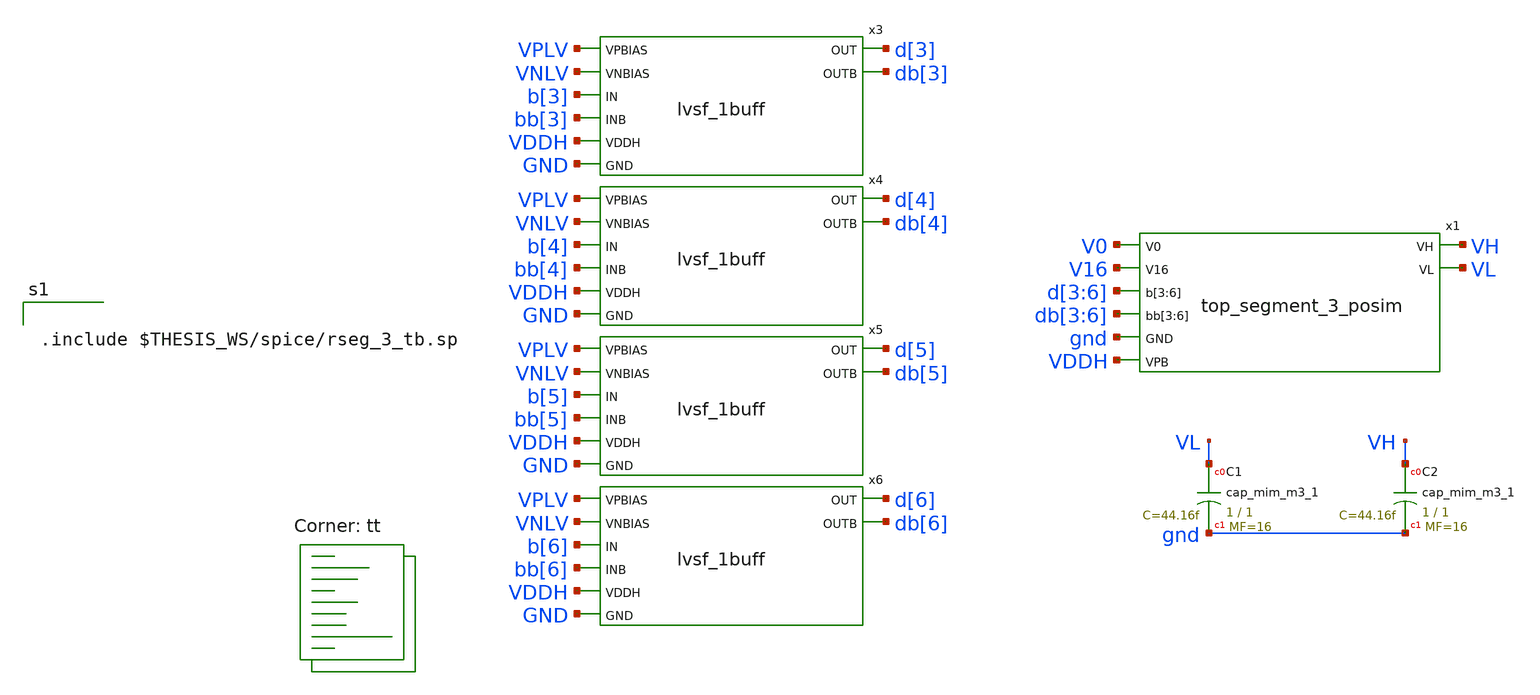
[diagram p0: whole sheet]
** sch_path: xschem/res_seg_3-tb.sch
**.subckt res_seg_3-tb
XC1 VL gnd sky130_fd_pr__cap_mim_m3_1 W=1 L=1 MF=16 m=16
XC2 VH gnd sky130_fd_pr__cap_mim_m3_1 W=1 L=1 MF=16 m=16
x3 VPLV VNLV b[3] bb[3] d[3] db[3] VDDH GND lvsf_1buff
x4 VPLV VNLV b[4] bb[4] d[4] db[4] VDDH GND lvsf_1buff
x5 VPLV VNLV b[5] bb[5] d[5] db[5] VDDH GND lvsf_1buff
x6 VPLV VNLV b[6] bb[6] d[6] db[6] VDDH GND lvsf_1buff
x1 V0 V16 d[3] d[4] d[5] d[6] db[3] db[4] db[5] db[6] VH VL gnd VDDH top_segment_3_posim
**** begin user architecture code
.lib $::SKYWATER_MODELS/sky130.lib.spice tt


.include $THESIS_WS/spice/rseg_3_tb.sp

**** end user architecture code
**.ends

* expanding   symbol:  lvsf_1buff.sym # of pins=8
** sym_path: xschem/lvsf_1buff.sym
** sch_path: xschem/lvsf_1buff.sch
.subckt lvsf_1buff VPBIAS VNBIAS IN INB OUT OUTB VDDH GND
*.ipin IN
*.ipin INB
*.opin OUT
*.ipin VDDH
*.ipin GND
*.ipin VPBIAS
*.ipin VNBIAS
*.opin OUTB
XM13 n1 IN GND GND sky130_fd_pr__nfet_01v8 L=0.15 W=3 nf=1 ad='int((nf+1)/2) * W/nf * 0.29' as='int((nf+2)/2) * W/nf * 0.29'
+ pd='2*int((nf+1)/2) * (W/nf + 0.29)' ps='2*int((nf+2)/2) * (W/nf + 0.29)' nrd='0.29 / W' nrs='0.29 / W'
+ sa=0 sb=0 sd=0 mult=1 m=1
XM1 net2 VPBIAS VDDH VDDH sky130_fd_pr__pfet_g5v0d10v5 L=0.8 W=1 nf=1 ad='int((nf+1)/2) * W/nf * 0.29'
+ as='int((nf+2)/2) * W/nf * 0.29' pd='2*int((nf+1)/2) * (W/nf + 0.29)' ps='2*int((nf+2)/2) * (W/nf + 0.29)'
+ nrd='0.29 / W' nrs='0.29 / W' sa=0 sb=0 sd=0 mult=1 m=1
XM2 net1 VPBIAS VDDH VDDH sky130_fd_pr__pfet_g5v0d10v5 L=0.8 W=1 nf=1 ad='int((nf+1)/2) * W/nf * 0.29'
+ as='int((nf+2)/2) * W/nf * 0.29' pd='2*int((nf+1)/2) * (W/nf + 0.29)' ps='2*int((nf+2)/2) * (W/nf + 0.29)'
+ nrd='0.29 / W' nrs='0.29 / W' sa=0 sb=0 sd=0 mult=1 m=1
XM3 OUTPB OUTP net2 VDDH sky130_fd_pr__pfet_g5v0d10v5 L=0.8 W=1 nf=1 ad='int((nf+1)/2) * W/nf * 0.29'
+ as='int((nf+2)/2) * W/nf * 0.29' pd='2*int((nf+1)/2) * (W/nf + 0.29)' ps='2*int((nf+2)/2) * (W/nf + 0.29)'
+ nrd='0.29 / W' nrs='0.29 / W' sa=0 sb=0 sd=0 mult=1 m=1
XM4 OUTP OUTPB net1 VDDH sky130_fd_pr__pfet_g5v0d10v5 L=0.8 W=1 nf=1 ad='int((nf+1)/2) * W/nf * 0.29'
+ as='int((nf+2)/2) * W/nf * 0.29' pd='2*int((nf+1)/2) * (W/nf + 0.29)' ps='2*int((nf+2)/2) * (W/nf + 0.29)'
+ nrd='0.29 / W' nrs='0.29 / W' sa=0 sb=0 sd=0 mult=1 m=1
XM5 OUTPB VNBIAS n1 GND sky130_fd_pr__nfet_g5v0d10v5 L=1 W=1 nf=1 ad='int((nf+1)/2) * W/nf * 0.29' as='int((nf+2)/2) * W/nf * 0.29'
+ pd='2*int((nf+1)/2) * (W/nf + 0.29)' ps='2*int((nf+2)/2) * (W/nf + 0.29)' nrd='0.29 / W' nrs='0.29 / W'
+ sa=0 sb=0 sd=0 mult=1 m=1
XM6 OUTP VNBIAS n2 GND sky130_fd_pr__nfet_g5v0d10v5 L=1 W=1 nf=1 ad='int((nf+1)/2) * W/nf * 0.29' as='int((nf+2)/2) * W/nf * 0.29'
+ pd='2*int((nf+1)/2) * (W/nf + 0.29)' ps='2*int((nf+2)/2) * (W/nf + 0.29)' nrd='0.29 / W' nrs='0.29 / W'
+ sa=0 sb=0 sd=0 mult=1 m=1
XM7 n2 INB GND GND sky130_fd_pr__nfet_01v8 L=0.15 W=3 nf=1 ad='int((nf+1)/2) * W/nf * 0.29' as='int((nf+2)/2) * W/nf * 0.29'
+ pd='2*int((nf+1)/2) * (W/nf + 0.29)' ps='2*int((nf+2)/2) * (W/nf + 0.29)' nrd='0.29 / W' nrs='0.29 / W'
+ sa=0 sb=0 sd=0 mult=1 m=1
x1 OUTP GND GND VDDH VDDH OUTB sky130_fd_sc_hvl__inv_1
x2 OUTB GND GND VDDH VDDH OUT sky130_fd_sc_hvl__inv_1
.ends

.end
